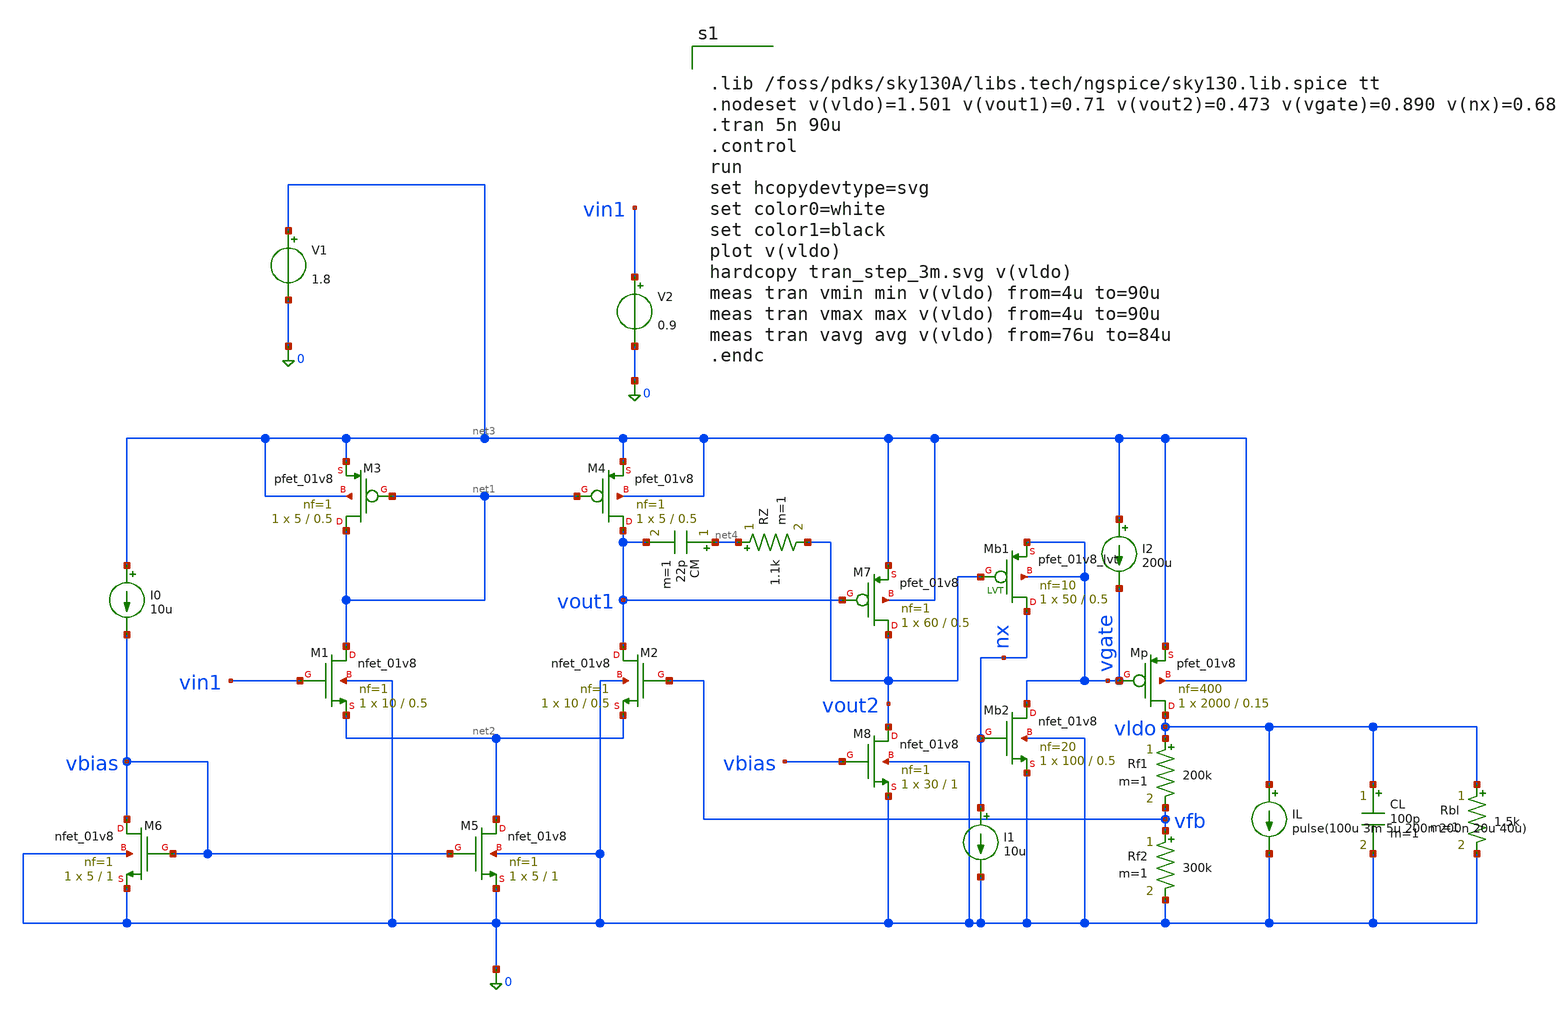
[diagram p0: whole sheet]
** sch_path: src/schematics/ldo_tran.sch
**.subckt ldo_tran
XM1 net1 vin1 net2 0 sky130_fd_pr__nfet_01v8 L=0.5 W=10 nf=1 ad='int((1 + 1)/2) * 10 / 1 * 0.29' as='int((1 + 2)/2) * 10 / 1 * 0.29'
+ pd='2*int((1 + 1)/2) * (10 / 1 + 0.29)' ps='2*int((1 + 2)/2) * (10 / 1 + 0.29)' nrd='0.29 / 10 ' nrs='0.29 / 10 '
+ sa=0 sb=0 sd=0 mult=1 m=1
XM2 vout1 vfb net2 0 sky130_fd_pr__nfet_01v8 L=0.5 W=10 nf=1 ad='int((1 + 1)/2) * 10 / 1 * 0.29' as='int((1 + 2)/2) * 10 / 1 * 0.29'
+ pd='2*int((1 + 1)/2) * (10 / 1 + 0.29)' ps='2*int((1 + 2)/2) * (10 / 1 + 0.29)' nrd='0.29 / 10 ' nrs='0.29 / 10 '
+ sa=0 sb=0 sd=0 mult=1 m=1
XM3 net1 net1 net3 net3 sky130_fd_pr__pfet_01v8 L=0.5 W=5 nf=1 ad='int((1 + 1)/2) * 5 / 1 * 0.29' as='int((1 + 2)/2) * 5 / 1 * 0.29'
+ pd='2*int((1 + 1)/2) * (5 / 1 + 0.29)' ps='2*int((1 + 2)/2) * (5 / 1 + 0.29)' nrd='0.29 / 5 ' nrs='0.29 / 5 '
+ sa=0 sb=0 sd=0 mult=1 m=1
XM4 vout1 net1 net3 net3 sky130_fd_pr__pfet_01v8 L=0.5 W=5 nf=1 ad='int((1 + 1)/2) * 5 / 1 * 0.29' as='int((1 + 2)/2) * 5 / 1 * 0.29'
+ pd='2*int((1 + 1)/2) * (5 / 1 + 0.29)' ps='2*int((1 + 2)/2) * (5 / 1 + 0.29)' nrd='0.29 / 5 ' nrs='0.29 / 5 '
+ sa=0 sb=0 sd=0 mult=1 m=1
XM5 net2 vbias 0 0 sky130_fd_pr__nfet_01v8 L=1 W=5 nf=1 ad='int((1 + 1)/2) * 5 / 1 * 0.29' as='int((1 + 2)/2) * 5 / 1 * 0.29'
+ pd='2*int((1 + 1)/2) * (5 / 1 + 0.29)' ps='2*int((1 + 2)/2) * (5 / 1 + 0.29)' nrd='0.29 / 5 ' nrs='0.29 / 5 '
+ sa=0 sb=0 sd=0 mult=1 m=1
XM6 vbias vbias 0 0 sky130_fd_pr__nfet_01v8 L=1 W=5 nf=1 ad='int((1 + 1)/2) * 5 / 1 * 0.29' as='int((1 + 2)/2) * 5 / 1 * 0.29'
+ pd='2*int((1 + 1)/2) * (5 / 1 + 0.29)' ps='2*int((1 + 2)/2) * (5 / 1 + 0.29)' nrd='0.29 / 5 ' nrs='0.29 / 5 '
+ sa=0 sb=0 sd=0 mult=1 m=1
I0 net3 vbias 10u
V1 net3 0 1.8
V2 vin1 0 0.9
XM7 vout2 vout1 net3 net3 sky130_fd_pr__pfet_01v8 L=0.5 W=60 nf=1 ad='int((1 + 1)/2) * 60 / 1 * 0.29'
+ as='int((1 + 2)/2) * 60 / 1 * 0.29' pd='2*int((1 + 1)/2) * (60 / 1 + 0.29)' ps='2*int((1 + 2)/2) * (60 / 1 + 0.29)'
+ nrd='0.29 / 60 ' nrs='0.29 / 60 ' sa=0 sb=0 sd=0 mult=1 m=1
XM8 vout2 vbias 0 0 sky130_fd_pr__nfet_01v8 L=1 W=30 nf=1 ad='int((1 + 1)/2) * 30 / 1 * 0.29' as='int((1 + 2)/2) * 30 / 1 * 0.29'
+ pd='2*int((1 + 1)/2) * (30 / 1 + 0.29)' ps='2*int((1 + 2)/2) * (30 / 1 + 0.29)' nrd='0.29 / 30 ' nrs='0.29 / 30 '
+ sa=0 sb=0 sd=0 mult=1 m=1
CM net4 vout1 22p m=1
RZ net4 vout2 1.1k m=1
Rf1 vldo vfb 200k m=1
Rf2 vfb 0 300k m=1
CL vldo 0 100p m=1
IL vldo 0 pulse(100u 3m 5u 200n 200n 20u 40u)
XMp vldo vgate net3 net3 sky130_fd_pr__pfet_01v8 L=0.15 W=2000 nf=400 ad='int((400 + 1)/2) * 2000 / 400 * 0.29'
+ as='int((400 + 2)/2) * 2000 / 400 * 0.29' pd='2*int((400 + 1)/2) * (2000 / 400 + 0.29)' ps='2*int((400 + 2)/2) * (2000 / 400 + 0.29)'
+ nrd='0.29 / 2000 ' nrs='0.29 / 2000 ' sa=0 sb=0 sd=0 mult=1 m=1
XMb2 vgate nx 0 0 sky130_fd_pr__nfet_01v8 L=0.5 W=100 nf=20 ad='int((20 + 1)/2) * 100 / 20 * 0.29' as='int((20 + 2)/2) * 100 / 20 * 0.29'
+ pd='2*int((20 + 1)/2) * (100 / 20 + 0.29)' ps='2*int((20 + 2)/2) * (100 / 20 + 0.29)' nrd='0.29 / 100 '
+ nrs='0.29 / 100 ' sa=0 sb=0 sd=0 mult=1 m=1
I1 nx 0 10u
I2 net3 vgate 200u
XMb1 nx vout2 vgate vgate sky130_fd_pr__pfet_01v8_lvt L=0.5 W=50 nf=10 ad='int((10 + 1)/2) * 50 / 10 * 0.29'
+ as='int((10 + 2)/2) * 50 / 10 * 0.29' pd='2*int((10 + 1)/2) * (50 / 10 + 0.29)' ps='2*int((10 + 2)/2) * (50 / 10 + 0.29)'
+ nrd='0.29 / 50 ' nrs='0.29 / 50 ' sa=0 sb=0 sd=0 mult=1 m=1
Rbl vldo 0 1.5k m=1
**** begin user architecture code


.lib /foss/pdks/sky130A/libs.tech/ngspice/sky130.lib.spice tt
.nodeset v(vldo)=1.501 v(vout1)=0.71 v(vout2)=0.473 v(vgate)=0.890 v(nx)=0.68
.tran 5n 90u
.control
run
set hcopydevtype=svg
set color0=white
set color1=black
plot v(vldo)
hardcopy tran_step_3m.svg v(vldo)
meas tran vmin min v(vldo) from=4u to=90u
meas tran vmax max v(vldo) from=4u to=90u
meas tran vavg avg v(vldo) from=76u to=84u
.endc


**** end user architecture code
**.ends
.end
